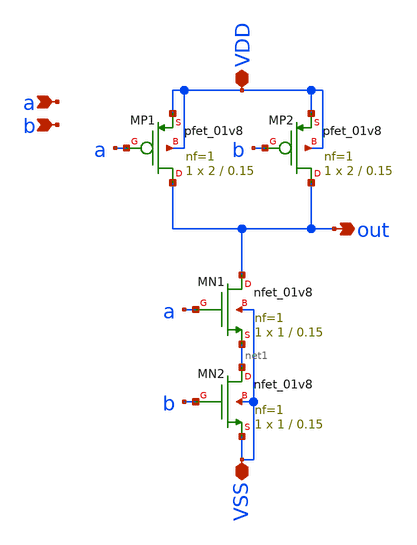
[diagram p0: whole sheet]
** sch_path: xsch/ip/nand2/nand2.sch
**.subckt nand2 a out VDD VSS b
*.ipin a
*.opin out
*.iopin VDD
*.iopin VSS
*.ipin b
XMN1 out a net1 VSS sky130_fd_pr__nfet_01v8 L=0.15 W=1 nf=1 ad='int((1 + 1)/2) * 1 / 1 * 0.29' as='int((1 + 2)/2) * 1 / 1 * 0.29'
+ pd='2*int((1 + 1)/2) * (1 / 1 + 0.29)' ps='2*int((1 + 2)/2) * (1 / 1 + 0.29)' nrd='0.29 / 1 ' nrs='0.29 / 1 '
+ sa=0 sb=0 sd=0 mult=1 m=1
XMP1 out a VDD VDD sky130_fd_pr__pfet_01v8 L=0.15 W=2 nf=1 ad='int((nf+1)/2) * W/nf * 0.29' as='int((nf+2)/2) * W/nf * 0.29'
+ pd='2*int((nf+1)/2) * (W/nf + 0.29)' ps='2*int((nf+2)/2) * (W/nf + 0.29)' nrd='0.29 / W' nrs='0.29 / W'
+ sa=0 sb=0 sd=0 mult=1 m=1
XMP2 out b VDD VDD sky130_fd_pr__pfet_01v8 L=0.15 W=2 nf=1 ad='int((nf+1)/2) * W/nf * 0.29' as='int((nf+2)/2) * W/nf * 0.29'
+ pd='2*int((nf+1)/2) * (W/nf + 0.29)' ps='2*int((nf+2)/2) * (W/nf + 0.29)' nrd='0.29 / W' nrs='0.29 / W'
+ sa=0 sb=0 sd=0 mult=1 m=1
XMN2 net1 b VSS VSS sky130_fd_pr__nfet_01v8 L=0.15 W=1 nf=1 ad='int((1 + 1)/2) * 1 / 1 * 0.29' as='int((1 + 2)/2) * 1 / 1 * 0.29'
+ pd='2*int((1 + 1)/2) * (1 / 1 + 0.29)' ps='2*int((1 + 2)/2) * (1 / 1 + 0.29)' nrd='0.29 / 1 ' nrs='0.29 / 1 '
+ sa=0 sb=0 sd=0 mult=1 m=1
**.ends
.end
